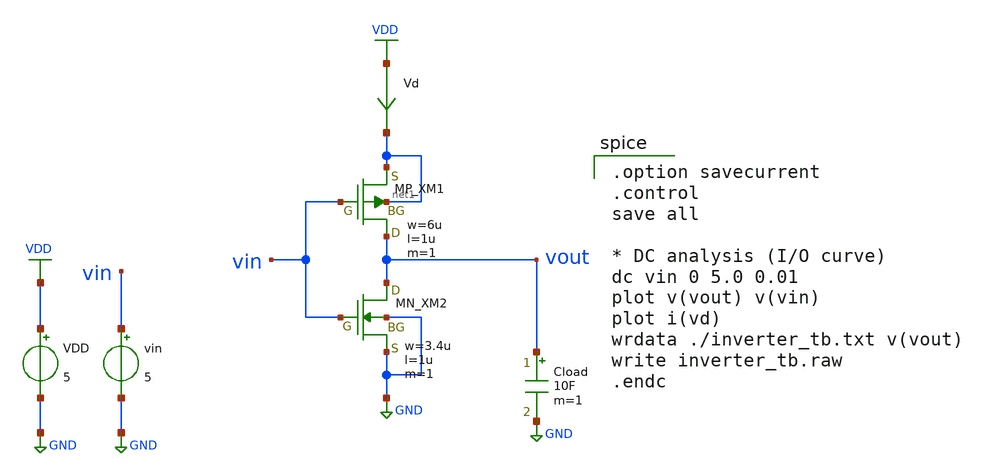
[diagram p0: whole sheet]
** sch_path: inverter/inverter_Shunsuke_Fujii_tb.sch
**.subckt inverter_Shunsuke_Fujii_tb
XXM1 vout vin net1 net1 PMOS w=6u l=1u nrd=0 nrs=0 m=1
XXM2 vout vin GND GND NMOS w=3.4u l=1u nrd=0 nrs=0 m=1
vin vin GND 5
VDD VDD GND 5
Cload vout GND 10F m=1
Vd VDD net1 0
.save i(vd)
**** begin user architecture code
 .include $::LIB/ip62_models

.option savecurrent
.control
save all

* DC analysis (I/O curve)
dc vin 0 5.0 0.01
plot v(vout) v(vin)
plot i(vd)
wrdata ./inverter_tb.txt v(vout)
write inverter_tb.raw
.endc

**** end user architecture code
**.ends
.GLOBAL GND
.GLOBAL VDD
.end
